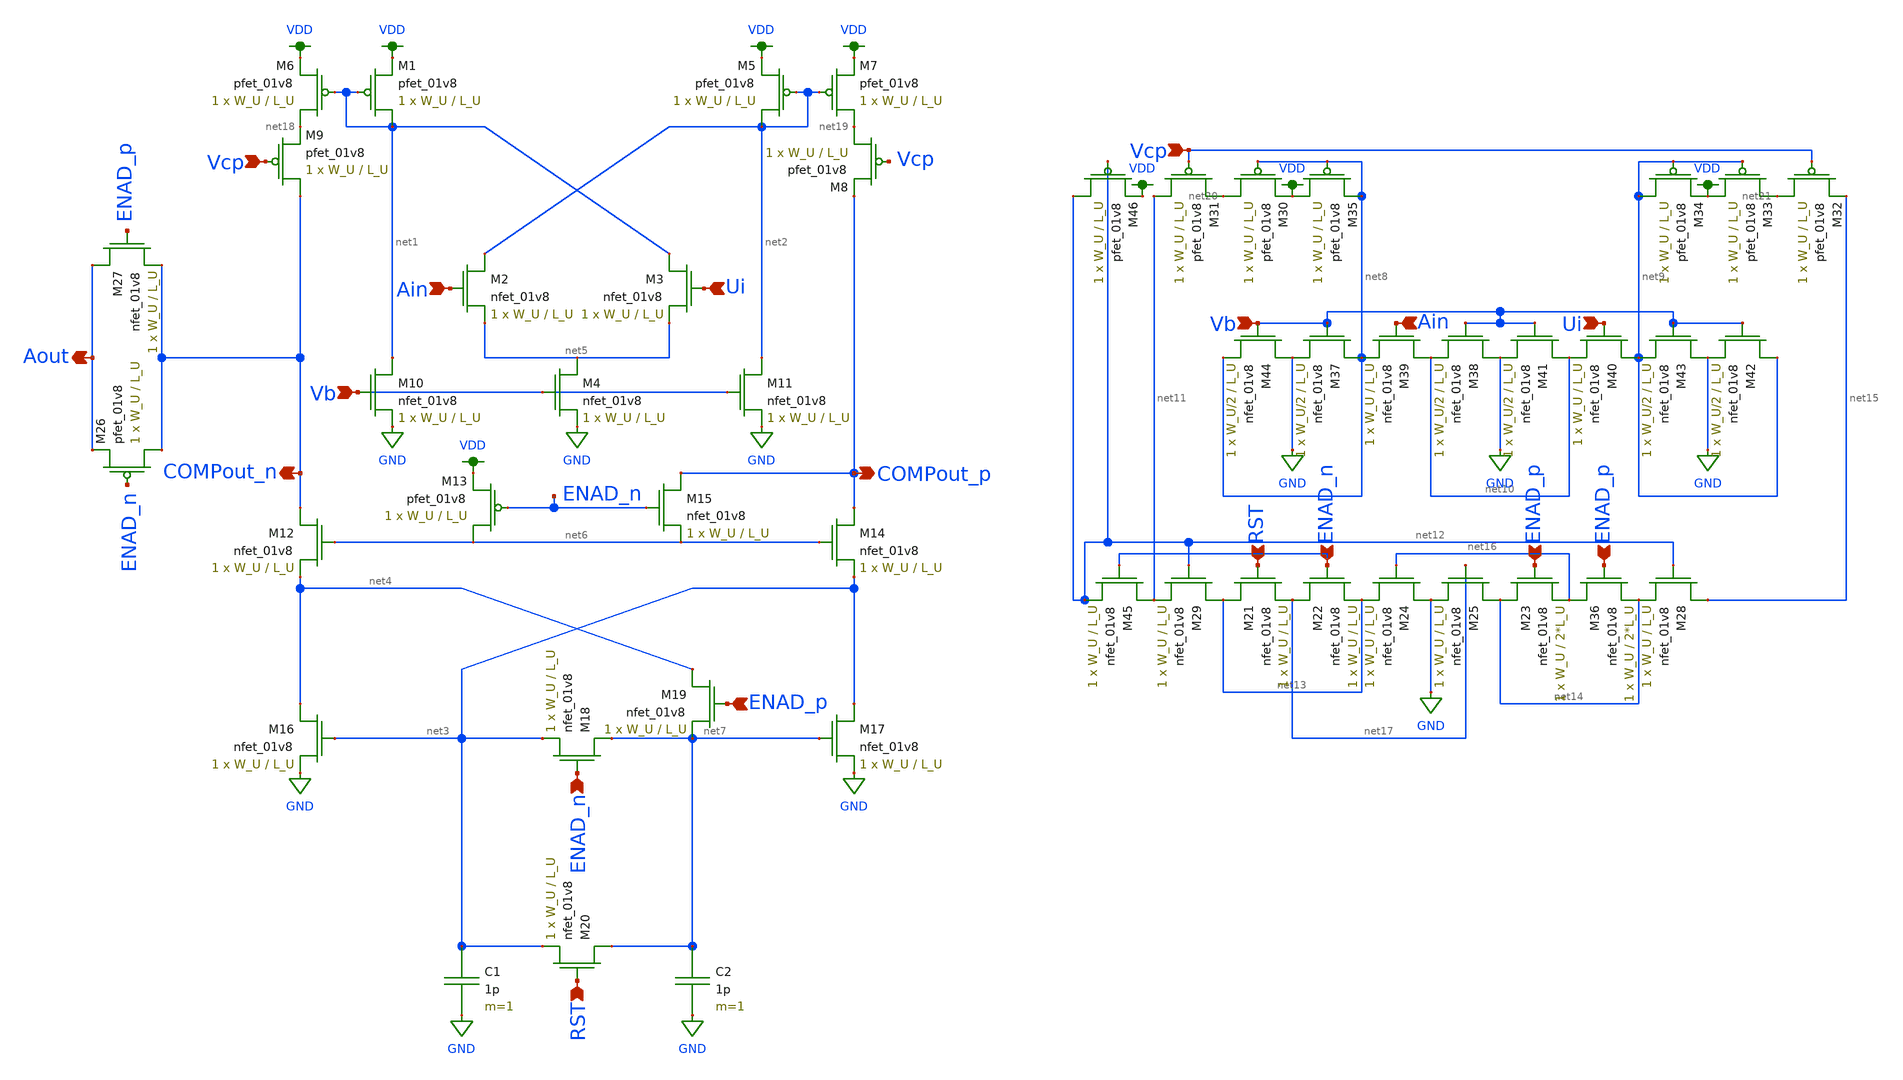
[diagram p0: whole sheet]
** sch_path: schematics/comp_lds.sch
**.subckt comp_lds Ain Vcp Vb Aout COMPout_n COMPout_p ENAD_n RST Ui ENAD_p RST ENAD_n ENAD_p Vcp Vb
*+ Ain Ui ENAD_p
*.ipin Ain
*.ipin Vcp
*.ipin Vb
*.opin Aout
*.opin COMPout_n
*.opin COMPout_p
*.ipin ENAD_n
*.ipin RST
*.ipin Ui
*.ipin ENAD_p
*.ipin RST
*.ipin ENAD_n
*.ipin ENAD_p
*.ipin Vcp
*.ipin Vb
*.ipin Ain
*.ipin Ui
*.ipin ENAD_p
XM1 net1 net1 VDD VDD sky130_fd_pr__pfet_01v8 L=L_U W=W_U nf=1 ad='int((nf+1)/2) * W/nf * 0.29' as='int((nf+2)/2) * W/nf * 0.29'
+ pd='2*int((nf+1)/2) * (W/nf + 0.29)' ps='2*int((nf+2)/2) * (W/nf + 0.29)' nrd='0.29 / W' nrs='0.29 / W'
+ sa=0 sb=0 sd=0 mult=1 m=1
XM2 net2 Ain net5 GND sky130_fd_pr__nfet_01v8 L=L_U W=W_U nf=1 ad='int((nf+1)/2) * W/nf * 0.29' as='int((nf+2)/2) * W/nf * 0.29'
+ pd='2*int((nf+1)/2) * (W/nf + 0.29)' ps='2*int((nf+2)/2) * (W/nf + 0.29)' nrd='0.29 / W' nrs='0.29 / W'
+ sa=0 sb=0 sd=0 mult=1 m=1
XM3 net1 Ui net5 GND sky130_fd_pr__nfet_01v8 L=L_U W=W_U nf=1 ad='int((nf+1)/2) * W/nf * 0.29' as='int((nf+2)/2) * W/nf * 0.29'
+ pd='2*int((nf+1)/2) * (W/nf + 0.29)' ps='2*int((nf+2)/2) * (W/nf + 0.29)' nrd='0.29 / W' nrs='0.29 / W'
+ sa=0 sb=0 sd=0 mult=1 m=1
XM4 net5 Vb GND GND sky130_fd_pr__nfet_01v8 L=L_U W=W_U nf=1 ad='int((nf+1)/2) * W/nf * 0.29' as='int((nf+2)/2) * W/nf * 0.29'
+ pd='2*int((nf+1)/2) * (W/nf + 0.29)' ps='2*int((nf+2)/2) * (W/nf + 0.29)' nrd='0.29 / W' nrs='0.29 / W'
+ sa=0 sb=0 sd=0 mult=1 m=1
XM5 net2 net2 VDD VDD sky130_fd_pr__pfet_01v8 L=L_U W=W_U nf=1 ad='int((nf+1)/2) * W/nf * 0.29' as='int((nf+2)/2) * W/nf * 0.29'
+ pd='2*int((nf+1)/2) * (W/nf + 0.29)' ps='2*int((nf+2)/2) * (W/nf + 0.29)' nrd='0.29 / W' nrs='0.29 / W'
+ sa=0 sb=0 sd=0 mult=1 m=1
XM6 net18 net1 VDD VDD sky130_fd_pr__pfet_01v8 L=L_U W=W_U nf=1 ad='int((nf+1)/2) * W/nf * 0.29' as='int((nf+2)/2) * W/nf * 0.29'
+ pd='2*int((nf+1)/2) * (W/nf + 0.29)' ps='2*int((nf+2)/2) * (W/nf + 0.29)' nrd='0.29 / W' nrs='0.29 / W'
+ sa=0 sb=0 sd=0 mult=1 m=1
XM7 net19 net2 VDD VDD sky130_fd_pr__pfet_01v8 L=L_U W=W_U nf=1 ad='int((nf+1)/2) * W/nf * 0.29' as='int((nf+2)/2) * W/nf * 0.29'
+ pd='2*int((nf+1)/2) * (W/nf + 0.29)' ps='2*int((nf+2)/2) * (W/nf + 0.29)' nrd='0.29 / W' nrs='0.29 / W'
+ sa=0 sb=0 sd=0 mult=1 m=1
XM8 net19 Vcp COMPout_p VDD sky130_fd_pr__pfet_01v8 L=L_U W=W_U nf=1 ad='int((nf+1)/2) * W/nf * 0.29'
+ as='int((nf+2)/2) * W/nf * 0.29' pd='2*int((nf+1)/2) * (W/nf + 0.29)' ps='2*int((nf+2)/2) * (W/nf + 0.29)'
+ nrd='0.29 / W' nrs='0.29 / W' sa=0 sb=0 sd=0 mult=1 m=1
XM9 COMPout_n Vcp net18 VDD sky130_fd_pr__pfet_01v8 L=L_U W=W_U nf=1 ad='int((nf+1)/2) * W/nf * 0.29'
+ as='int((nf+2)/2) * W/nf * 0.29' pd='2*int((nf+1)/2) * (W/nf + 0.29)' ps='2*int((nf+2)/2) * (W/nf + 0.29)'
+ nrd='0.29 / W' nrs='0.29 / W' sa=0 sb=0 sd=0 mult=1 m=1
XM10 net1 Vb GND GND sky130_fd_pr__nfet_01v8 L=L_U W=W_U nf=1 ad='int((nf+1)/2) * W/nf * 0.29' as='int((nf+2)/2) * W/nf * 0.29'
+ pd='2*int((nf+1)/2) * (W/nf + 0.29)' ps='2*int((nf+2)/2) * (W/nf + 0.29)' nrd='0.29 / W' nrs='0.29 / W'
+ sa=0 sb=0 sd=0 mult=1 m=1
XM11 net2 Vb GND GND sky130_fd_pr__nfet_01v8 L=L_U W=W_U nf=1 ad='int((nf+1)/2) * W/nf * 0.29' as='int((nf+2)/2) * W/nf * 0.29'
+ pd='2*int((nf+1)/2) * (W/nf + 0.29)' ps='2*int((nf+2)/2) * (W/nf + 0.29)' nrd='0.29 / W' nrs='0.29 / W'
+ sa=0 sb=0 sd=0 mult=1 m=1
XM12 COMPout_n net6 net4 GND sky130_fd_pr__nfet_01v8 L=L_U W=W_U nf=1 ad='int((nf+1)/2) * W/nf * 0.29'
+ as='int((nf+2)/2) * W/nf * 0.29' pd='2*int((nf+1)/2) * (W/nf + 0.29)' ps='2*int((nf+2)/2) * (W/nf + 0.29)'
+ nrd='0.29 / W' nrs='0.29 / W' sa=0 sb=0 sd=0 mult=1 m=1
XM13 net6 ENAD_n VDD VDD sky130_fd_pr__pfet_01v8 L=L_U W=W_U nf=1 ad='int((nf+1)/2) * W/nf * 0.29' as='int((nf+2)/2) * W/nf * 0.29'
+ pd='2*int((nf+1)/2) * (W/nf + 0.29)' ps='2*int((nf+2)/2) * (W/nf + 0.29)' nrd='0.29 / W' nrs='0.29 / W'
+ sa=0 sb=0 sd=0 mult=1 m=1
XM14 COMPout_p net6 net3 GND sky130_fd_pr__nfet_01v8 L=L_U W=W_U nf=1 ad='int((nf+1)/2) * W/nf * 0.29'
+ as='int((nf+2)/2) * W/nf * 0.29' pd='2*int((nf+1)/2) * (W/nf + 0.29)' ps='2*int((nf+2)/2) * (W/nf + 0.29)'
+ nrd='0.29 / W' nrs='0.29 / W' sa=0 sb=0 sd=0 mult=1 m=1
XM15 COMPout_p ENAD_n net6 GND sky130_fd_pr__nfet_01v8 L=L_U W=W_U nf=1 ad='int((nf+1)/2) * W/nf * 0.29'
+ as='int((nf+2)/2) * W/nf * 0.29' pd='2*int((nf+1)/2) * (W/nf + 0.29)' ps='2*int((nf+2)/2) * (W/nf + 0.29)'
+ nrd='0.29 / W' nrs='0.29 / W' sa=0 sb=0 sd=0 mult=1 m=1
XM16 net4 net3 GND GND sky130_fd_pr__nfet_01v8 L=L_U W=W_U nf=1 ad='int((nf+1)/2) * W/nf * 0.29' as='int((nf+2)/2) * W/nf * 0.29'
+ pd='2*int((nf+1)/2) * (W/nf + 0.29)' ps='2*int((nf+2)/2) * (W/nf + 0.29)' nrd='0.29 / W' nrs='0.29 / W'
+ sa=0 sb=0 sd=0 mult=1 m=1
XM17 net3 net7 GND GND sky130_fd_pr__nfet_01v8 L=L_U W=W_U nf=1 ad='int((nf+1)/2) * W/nf * 0.29' as='int((nf+2)/2) * W/nf * 0.29'
+ pd='2*int((nf+1)/2) * (W/nf + 0.29)' ps='2*int((nf+2)/2) * (W/nf + 0.29)' nrd='0.29 / W' nrs='0.29 / W'
+ sa=0 sb=0 sd=0 mult=1 m=1
XM18 net7 ENAD_n net3 GND sky130_fd_pr__nfet_01v8 L=L_U W=W_U nf=1 ad='int((nf+1)/2) * W/nf * 0.29' as='int((nf+2)/2) * W/nf * 0.29'
+ pd='2*int((nf+1)/2) * (W/nf + 0.29)' ps='2*int((nf+2)/2) * (W/nf + 0.29)' nrd='0.29 / W' nrs='0.29 / W'
+ sa=0 sb=0 sd=0 mult=1 m=1
XM19 net4 ENAD_p net7 GND sky130_fd_pr__nfet_01v8 L=L_U W=W_U nf=1 ad='int((nf+1)/2) * W/nf * 0.29' as='int((nf+2)/2) * W/nf * 0.29'
+ pd='2*int((nf+1)/2) * (W/nf + 0.29)' ps='2*int((nf+2)/2) * (W/nf + 0.29)' nrd='0.29 / W' nrs='0.29 / W'
+ sa=0 sb=0 sd=0 mult=1 m=1
XM20 net7 RST net3 GND sky130_fd_pr__nfet_01v8 L=L_U W=W_U nf=1 ad='int((nf+1)/2) * W/nf * 0.29' as='int((nf+2)/2) * W/nf * 0.29'
+ pd='2*int((nf+1)/2) * (W/nf + 0.29)' ps='2*int((nf+2)/2) * (W/nf + 0.29)' nrd='0.29 / W' nrs='0.29 / W'
+ sa=0 sb=0 sd=0 mult=1 m=1
C1 net3 GND 1p m=1
C2 net7 GND 1p m=1
XM26 COMPout_n ENAD_n Aout VDD sky130_fd_pr__pfet_01v8 L=L_U W=W_U nf=1 ad='int((nf+1)/2) * W/nf * 0.29'
+ as='int((nf+2)/2) * W/nf * 0.29' pd='2*int((nf+1)/2) * (W/nf + 0.29)' ps='2*int((nf+2)/2) * (W/nf + 0.29)'
+ nrd='0.29 / W' nrs='0.29 / W' sa=0 sb=0 sd=0 mult=1 m=1
XM27 Aout ENAD_p COMPout_n GND sky130_fd_pr__nfet_01v8 L=L_U W=W_U nf=1 ad='int((nf+1)/2) * W/nf * 0.29'
+ as='int((nf+2)/2) * W/nf * 0.29' pd='2*int((nf+1)/2) * (W/nf + 0.29)' ps='2*int((nf+2)/2) * (W/nf + 0.29)'
+ nrd='0.29 / W' nrs='0.29 / W' sa=0 sb=0 sd=0 mult=1 m=1
XM21 net13 RST net17 GND sky130_fd_pr__nfet_01v8 L=L_U W=W_U nf=1 ad='int((nf+1)/2) * W/nf * 0.29' as='int((nf+2)/2) * W/nf * 0.29'
+ pd='2*int((nf+1)/2) * (W/nf + 0.29)' ps='2*int((nf+2)/2) * (W/nf + 0.29)' nrd='0.29 / W' nrs='0.29 / W'
+ sa=0 sb=0 sd=0 mult=1 m=1
XM22 net17 ENAD_n net13 GND sky130_fd_pr__nfet_01v8 L=L_U W=W_U nf=1 ad='int((nf+1)/2) * W/nf * 0.29'
+ as='int((nf+2)/2) * W/nf * 0.29' pd='2*int((nf+1)/2) * (W/nf + 0.29)' ps='2*int((nf+2)/2) * (W/nf + 0.29)'
+ nrd='0.29 / W' nrs='0.29 / W' sa=0 sb=0 sd=0 mult=1 m=1
XM23 net14 ENAD_p net16 GND sky130_fd_pr__nfet_01v8 L=2*L_U W=W_U nf=1 ad='int((nf+1)/2) * W/nf * 0.29'
+ as='int((nf+2)/2) * W/nf * 0.29' pd='2*int((nf+1)/2) * (W/nf + 0.29)' ps='2*int((nf+2)/2) * (W/nf + 0.29)'
+ nrd='0.29 / W' nrs='0.29 / W' sa=0 sb=0 sd=0 mult=1 m=1
XM24 GND net16 net13 GND sky130_fd_pr__nfet_01v8 L=L_U W=W_U nf=1 ad='int((nf+1)/2) * W/nf * 0.29' as='int((nf+2)/2) * W/nf * 0.29'
+ pd='2*int((nf+1)/2) * (W/nf + 0.29)' ps='2*int((nf+2)/2) * (W/nf + 0.29)' nrd='0.29 / W' nrs='0.29 / W'
+ sa=0 sb=0 sd=0 mult=1 m=1
XM25 net14 net17 GND GND sky130_fd_pr__nfet_01v8 L=L_U W=W_U nf=1 ad='int((nf+1)/2) * W/nf * 0.29' as='int((nf+2)/2) * W/nf * 0.29'
+ pd='2*int((nf+1)/2) * (W/nf + 0.29)' ps='2*int((nf+2)/2) * (W/nf + 0.29)' nrd='0.29 / W' nrs='0.29 / W'
+ sa=0 sb=0 sd=0 mult=1 m=1
XM28 net15 net12 net14 GND sky130_fd_pr__nfet_01v8 L=L_U W=W_U nf=1 ad='int((nf+1)/2) * W/nf * 0.29'
+ as='int((nf+2)/2) * W/nf * 0.29' pd='2*int((nf+1)/2) * (W/nf + 0.29)' ps='2*int((nf+2)/2) * (W/nf + 0.29)'
+ nrd='0.29 / W' nrs='0.29 / W' sa=0 sb=0 sd=0 mult=1 m=1
XM29 net13 net12 net11 GND sky130_fd_pr__nfet_01v8 L=L_U W=W_U nf=1 ad='int((nf+1)/2) * W/nf * 0.29'
+ as='int((nf+2)/2) * W/nf * 0.29' pd='2*int((nf+1)/2) * (W/nf + 0.29)' ps='2*int((nf+2)/2) * (W/nf + 0.29)'
+ nrd='0.29 / W' nrs='0.29 / W' sa=0 sb=0 sd=0 mult=1 m=1
XM30 net20 net8 VDD VDD sky130_fd_pr__pfet_01v8 L=L_U W=W_U nf=1 ad='int((nf+1)/2) * W/nf * 0.29' as='int((nf+2)/2) * W/nf * 0.29'
+ pd='2*int((nf+1)/2) * (W/nf + 0.29)' ps='2*int((nf+2)/2) * (W/nf + 0.29)' nrd='0.29 / W' nrs='0.29 / W'
+ sa=0 sb=0 sd=0 mult=1 m=1
XM31 net11 Vcp net20 VDD sky130_fd_pr__pfet_01v8 L=L_U W=W_U nf=1 ad='int((nf+1)/2) * W/nf * 0.29' as='int((nf+2)/2) * W/nf * 0.29'
+ pd='2*int((nf+1)/2) * (W/nf + 0.29)' ps='2*int((nf+2)/2) * (W/nf + 0.29)' nrd='0.29 / W' nrs='0.29 / W'
+ sa=0 sb=0 sd=0 mult=1 m=1
XM32 net21 Vcp net15 VDD sky130_fd_pr__pfet_01v8 L=L_U W=W_U nf=1 ad='int((nf+1)/2) * W/nf * 0.29' as='int((nf+2)/2) * W/nf * 0.29'
+ pd='2*int((nf+1)/2) * (W/nf + 0.29)' ps='2*int((nf+2)/2) * (W/nf + 0.29)' nrd='0.29 / W' nrs='0.29 / W'
+ sa=0 sb=0 sd=0 mult=1 m=1
XM33 VDD net9 net21 VDD sky130_fd_pr__pfet_01v8 L=L_U W=W_U nf=1 ad='int((nf+1)/2) * W/nf * 0.29' as='int((nf+2)/2) * W/nf * 0.29'
+ pd='2*int((nf+1)/2) * (W/nf + 0.29)' ps='2*int((nf+2)/2) * (W/nf + 0.29)' nrd='0.29 / W' nrs='0.29 / W'
+ sa=0 sb=0 sd=0 mult=1 m=1
XM34 net9 net9 VDD VDD sky130_fd_pr__pfet_01v8 L=L_U W=W_U nf=1 ad='int((nf+1)/2) * W/nf * 0.29' as='int((nf+2)/2) * W/nf * 0.29'
+ pd='2*int((nf+1)/2) * (W/nf + 0.29)' ps='2*int((nf+2)/2) * (W/nf + 0.29)' nrd='0.29 / W' nrs='0.29 / W'
+ sa=0 sb=0 sd=0 mult=1 m=1
XM35 VDD net8 net8 VDD sky130_fd_pr__pfet_01v8 L=L_U W=W_U nf=1 ad='int((nf+1)/2) * W/nf * 0.29' as='int((nf+2)/2) * W/nf * 0.29'
+ pd='2*int((nf+1)/2) * (W/nf + 0.29)' ps='2*int((nf+2)/2) * (W/nf + 0.29)' nrd='0.29 / W' nrs='0.29 / W'
+ sa=0 sb=0 sd=0 mult=1 m=1
XM37 net8 Vb GND GND sky130_fd_pr__nfet_01v8 L=L_U W=W_U/2 nf=1 ad='int((nf+1)/2) * W/nf * 0.29' as='int((nf+2)/2) * W/nf * 0.29'
+ pd='2*int((nf+1)/2) * (W/nf + 0.29)' ps='2*int((nf+2)/2) * (W/nf + 0.29)' nrd='0.29 / W' nrs='0.29 / W'
+ sa=0 sb=0 sd=0 mult=1 m=1
XM38 GND Vb net10 GND sky130_fd_pr__nfet_01v8 L=L_U W=W_U/2 nf=1 ad='int((nf+1)/2) * W/nf * 0.29' as='int((nf+2)/2) * W/nf * 0.29'
+ pd='2*int((nf+1)/2) * (W/nf + 0.29)' ps='2*int((nf+2)/2) * (W/nf + 0.29)' nrd='0.29 / W' nrs='0.29 / W'
+ sa=0 sb=0 sd=0 mult=1 m=1
XM39 net10 Ain net8 GND sky130_fd_pr__nfet_01v8 L=L_U W=W_U nf=1 ad='int((nf+1)/2) * W/nf * 0.29' as='int((nf+2)/2) * W/nf * 0.29'
+ pd='2*int((nf+1)/2) * (W/nf + 0.29)' ps='2*int((nf+2)/2) * (W/nf + 0.29)' nrd='0.29 / W' nrs='0.29 / W'
+ sa=0 sb=0 sd=0 mult=1 m=1
XM40 net9 Ui net10 GND sky130_fd_pr__nfet_01v8 L=L_U W=W_U nf=1 ad='int((nf+1)/2) * W/nf * 0.29' as='int((nf+2)/2) * W/nf * 0.29'
+ pd='2*int((nf+1)/2) * (W/nf + 0.29)' ps='2*int((nf+2)/2) * (W/nf + 0.29)' nrd='0.29 / W' nrs='0.29 / W'
+ sa=0 sb=0 sd=0 mult=1 m=1
XM41 net10 Vb GND GND sky130_fd_pr__nfet_01v8 L=L_U W=W_U/2 nf=1 ad='int((nf+1)/2) * W/nf * 0.29' as='int((nf+2)/2) * W/nf * 0.29'
+ pd='2*int((nf+1)/2) * (W/nf + 0.29)' ps='2*int((nf+2)/2) * (W/nf + 0.29)' nrd='0.29 / W' nrs='0.29 / W'
+ sa=0 sb=0 sd=0 mult=1 m=1
XM42 net9 Vb GND GND sky130_fd_pr__nfet_01v8 L=L_U W=W_U/2 nf=1 ad='int((nf+1)/2) * W/nf * 0.29' as='int((nf+2)/2) * W/nf * 0.29'
+ pd='2*int((nf+1)/2) * (W/nf + 0.29)' ps='2*int((nf+2)/2) * (W/nf + 0.29)' nrd='0.29 / W' nrs='0.29 / W'
+ sa=0 sb=0 sd=0 mult=1 m=1
XM43 GND Vb net9 GND sky130_fd_pr__nfet_01v8 L=L_U W=W_U/2 nf=1 ad='int((nf+1)/2) * W/nf * 0.29' as='int((nf+2)/2) * W/nf * 0.29'
+ pd='2*int((nf+1)/2) * (W/nf + 0.29)' ps='2*int((nf+2)/2) * (W/nf + 0.29)' nrd='0.29 / W' nrs='0.29 / W'
+ sa=0 sb=0 sd=0 mult=1 m=1
XM44 GND Vb net8 GND sky130_fd_pr__nfet_01v8 L=L_U W=W_U/2 nf=1 ad='int((nf+1)/2) * W/nf * 0.29' as='int((nf+2)/2) * W/nf * 0.29'
+ pd='2*int((nf+1)/2) * (W/nf + 0.29)' ps='2*int((nf+2)/2) * (W/nf + 0.29)' nrd='0.29 / W' nrs='0.29 / W'
+ sa=0 sb=0 sd=0 mult=1 m=1
XM46 net12 net12 VDD VDD sky130_fd_pr__pfet_01v8 L=L_U W=W_U nf=1 ad='int((nf+1)/2) * W/nf * 0.29' as='int((nf+2)/2) * W/nf * 0.29'
+ pd='2*int((nf+1)/2) * (W/nf + 0.29)' ps='2*int((nf+2)/2) * (W/nf + 0.29)' nrd='0.29 / W' nrs='0.29 / W'
+ sa=0 sb=0 sd=0 mult=1 m=1
XM36 net16 ENAD_p net14 GND sky130_fd_pr__nfet_01v8 L=2*L_U W=W_U nf=1 ad='int((nf+1)/2) * W/nf * 0.29'
+ as='int((nf+2)/2) * W/nf * 0.29' pd='2*int((nf+1)/2) * (W/nf + 0.29)' ps='2*int((nf+2)/2) * (W/nf + 0.29)'
+ nrd='0.29 / W' nrs='0.29 / W' sa=0 sb=0 sd=0 mult=1 m=1
XM45 net11 ENAD_n net12 GND sky130_fd_pr__nfet_01v8 L=L_U W=W_U nf=1 ad='int((nf+1)/2) * W/nf * 0.29'
+ as='int((nf+2)/2) * W/nf * 0.29' pd='2*int((nf+1)/2) * (W/nf + 0.29)' ps='2*int((nf+2)/2) * (W/nf + 0.29)'
+ nrd='0.29 / W' nrs='0.29 / W' sa=0 sb=0 sd=0 mult=1 m=1
**.ends
.GLOBAL VDD
.GLOBAL GND
.end
